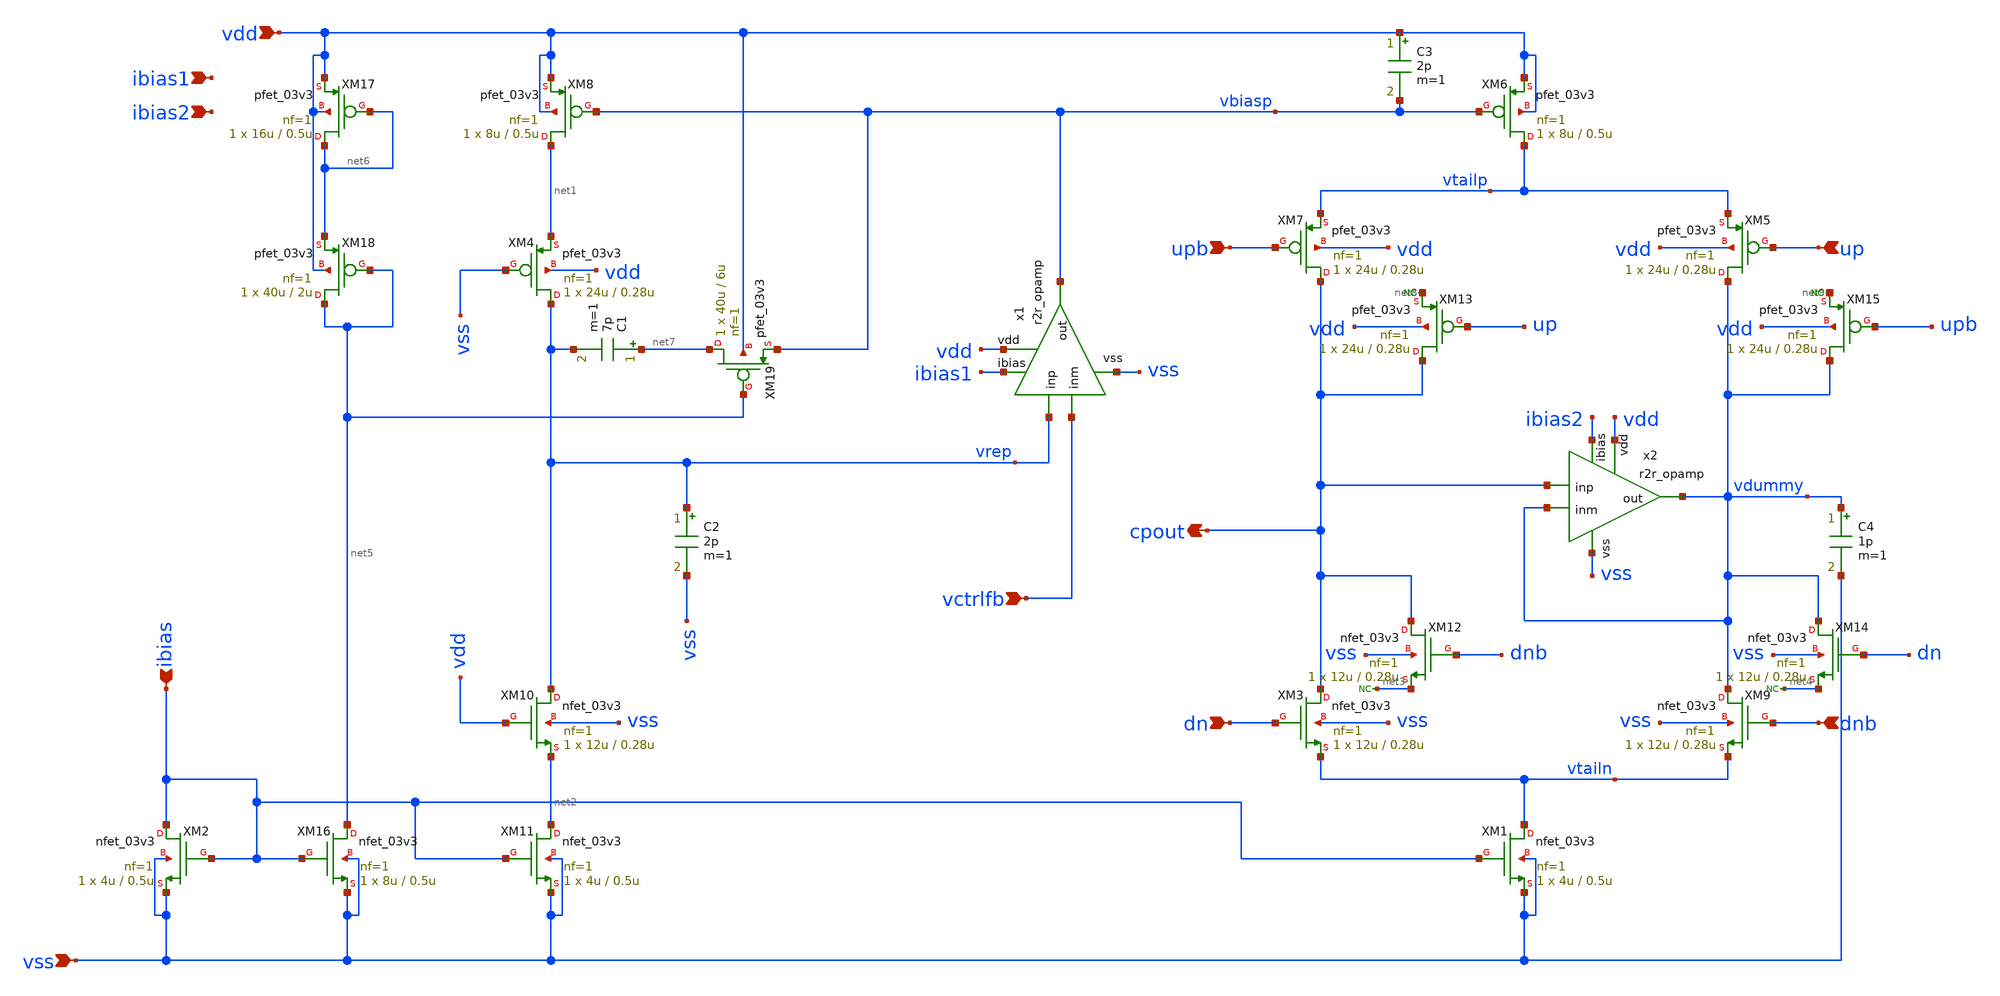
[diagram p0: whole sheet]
** sch_path: xschem/charge_pump_adv.sch
**.subckt charge_pump_adv vdd vss ibias dn upb up dnb cpout ibias1 ibias2 vctrlfb
*.ipin vdd
*.ipin vss
*.ipin ibias
*.ipin dn
*.ipin upb
*.ipin up
*.ipin dnb
*.opin cpout
*.ipin ibias1
*.ipin ibias2
*.ipin vctrlfb
XM1 vtailn ibias vss vss nfet_03v3 L=0.5u W=4u nf=1 ad='int((nf+1)/2) * W/nf * 0.18u' as='int((nf+2)/2) * W/nf * 0.18u'
+ pd='2*int((nf+1)/2) * (W/nf + 0.18u)' ps='2*int((nf+2)/2) * (W/nf + 0.18u)' nrd='0.18u / W' nrs='0.18u / W'
+ sa=0 sb=0 sd=0 m=1
XM2 ibias ibias vss vss nfet_03v3 L=0.5u W=4u nf=1 ad='int((nf+1)/2) * W/nf * 0.18u' as='int((nf+2)/2) * W/nf * 0.18u'
+ pd='2*int((nf+1)/2) * (W/nf + 0.18u)' ps='2*int((nf+2)/2) * (W/nf + 0.18u)' nrd='0.18u / W' nrs='0.18u / W'
+ sa=0 sb=0 sd=0 m=1
XM3 cpout dn vtailn vss nfet_03v3 L=0.28u W=12u nf=1 ad='int((nf+1)/2) * W/nf * 0.18u' as='int((nf+2)/2) * W/nf * 0.18u'
+ pd='2*int((nf+1)/2) * (W/nf + 0.18u)' ps='2*int((nf+2)/2) * (W/nf + 0.18u)' nrd='0.18u / W' nrs='0.18u / W'
+ sa=0 sb=0 sd=0 m=1
XM6 vtailp vbiasp vdd vdd pfet_03v3 L=0.5u W=8u nf=1 ad='int((nf+1)/2) * W/nf * 0.18u' as='int((nf+2)/2) * W/nf * 0.18u'
+ pd='2*int((nf+1)/2) * (W/nf + 0.18u)' ps='2*int((nf+2)/2) * (W/nf + 0.18u)' nrd='0.18u / W' nrs='0.18u / W'
+ sa=0 sb=0 sd=0 m=1
XM7 cpout upb vtailp vdd pfet_03v3 L=0.28u W=24u nf=1 ad='int((nf+1)/2) * W/nf * 0.18u' as='int((nf+2)/2) * W/nf * 0.18u'
+ pd='2*int((nf+1)/2) * (W/nf + 0.18u)' ps='2*int((nf+2)/2) * (W/nf + 0.18u)' nrd='0.18u / W' nrs='0.18u / W'
+ sa=0 sb=0 sd=0 m=1
XM8 net1 vbiasp vdd vdd pfet_03v3 L=0.5u W=8u nf=1 ad='int((nf+1)/2) * W/nf * 0.18u' as='int((nf+2)/2) * W/nf * 0.18u'
+ pd='2*int((nf+1)/2) * (W/nf + 0.18u)' ps='2*int((nf+2)/2) * (W/nf + 0.18u)' nrd='0.18u / W' nrs='0.18u / W'
+ sa=0 sb=0 sd=0 m=1
x1 vdd vbiasp ibias1 vrep vctrlfb vss r2r_opamp
XM5 vdummy up vtailp vdd pfet_03v3 L=0.28u W=24u nf=1 ad='int((nf+1)/2) * W/nf * 0.18u' as='int((nf+2)/2) * W/nf * 0.18u'
+ pd='2*int((nf+1)/2) * (W/nf + 0.18u)' ps='2*int((nf+2)/2) * (W/nf + 0.18u)' nrd='0.18u / W' nrs='0.18u / W'
+ sa=0 sb=0 sd=0 m=1
XM9 vdummy dnb vtailn vss nfet_03v3 L=0.28u W=12u nf=1 ad='int((nf+1)/2) * W/nf * 0.18u' as='int((nf+2)/2) * W/nf * 0.18u'
+ pd='2*int((nf+1)/2) * (W/nf + 0.18u)' ps='2*int((nf+2)/2) * (W/nf + 0.18u)' nrd='0.18u / W' nrs='0.18u / W'
+ sa=0 sb=0 sd=0 m=1
x2 vdd vdummy ibias2 cpout vdummy vss r2r_opamp
XM4 vrep vss net1 vdd pfet_03v3 L=0.28u W=24u nf=1 ad='int((nf+1)/2) * W/nf * 0.18u' as='int((nf+2)/2) * W/nf * 0.18u'
+ pd='2*int((nf+1)/2) * (W/nf + 0.18u)' ps='2*int((nf+2)/2) * (W/nf + 0.18u)' nrd='0.18u / W' nrs='0.18u / W'
+ sa=0 sb=0 sd=0 m=1
XM10 vrep vdd net2 vss nfet_03v3 L=0.28u W=12u nf=1 ad='int((nf+1)/2) * W/nf * 0.18u' as='int((nf+2)/2) * W/nf * 0.18u'
+ pd='2*int((nf+1)/2) * (W/nf + 0.18u)' ps='2*int((nf+2)/2) * (W/nf + 0.18u)' nrd='0.18u / W' nrs='0.18u / W'
+ sa=0 sb=0 sd=0 m=1
XM11 net2 ibias vss vss nfet_03v3 L=0.5u W=4u nf=1 ad='int((nf+1)/2) * W/nf * 0.18u' as='int((nf+2)/2) * W/nf * 0.18u'
+ pd='2*int((nf+1)/2) * (W/nf + 0.18u)' ps='2*int((nf+2)/2) * (W/nf + 0.18u)' nrd='0.18u / W' nrs='0.18u / W'
+ sa=0 sb=0 sd=0 m=1
XM12 cpout dnb net3 vss nfet_03v3 L=0.28u W=12u nf=1 ad='int((nf+1)/2) * W/nf * 0.18u' as='int((nf+2)/2) * W/nf * 0.18u'
+ pd='2*int((nf+1)/2) * (W/nf + 0.18u)' ps='2*int((nf+2)/2) * (W/nf + 0.18u)' nrd='0.18u / W' nrs='0.18u / W'
+ sa=0 sb=0 sd=0 m=1
XM13 cpout up net8 vdd pfet_03v3 L=0.28u W=24u nf=1 ad='int((nf+1)/2) * W/nf * 0.18u' as='int((nf+2)/2) * W/nf * 0.18u'
+ pd='2*int((nf+1)/2) * (W/nf + 0.18u)' ps='2*int((nf+2)/2) * (W/nf + 0.18u)' nrd='0.18u / W' nrs='0.18u / W'
+ sa=0 sb=0 sd=0 m=1
C1 net7 vrep 7p m=1
C4 vdummy vss 1p m=1
C3 vdd vbiasp 2p m=1
XM14 vdummy dn net4 vss nfet_03v3 L=0.28u W=12u nf=1 ad='int((nf+1)/2) * W/nf * 0.18u' as='int((nf+2)/2) * W/nf * 0.18u'
+ pd='2*int((nf+1)/2) * (W/nf + 0.18u)' ps='2*int((nf+2)/2) * (W/nf + 0.18u)' nrd='0.18u / W' nrs='0.18u / W'
+ sa=0 sb=0 sd=0 m=1
XM15 vdummy upb net9 vdd pfet_03v3 L=0.28u W=24u nf=1 ad='int((nf+1)/2) * W/nf * 0.18u' as='int((nf+2)/2) * W/nf * 0.18u'
+ pd='2*int((nf+1)/2) * (W/nf + 0.18u)' ps='2*int((nf+2)/2) * (W/nf + 0.18u)' nrd='0.18u / W' nrs='0.18u / W'
+ sa=0 sb=0 sd=0 m=1
* noconn #net3
* noconn #net4
* noconn #net9
* noconn #net8
XM16 net5 ibias vss vss nfet_03v3 L=0.5u W=8u nf=1 ad='int((nf+1)/2) * W/nf * 0.18u' as='int((nf+2)/2) * W/nf * 0.18u'
+ pd='2*int((nf+1)/2) * (W/nf + 0.18u)' ps='2*int((nf+2)/2) * (W/nf + 0.18u)' nrd='0.18u / W' nrs='0.18u / W'
+ sa=0 sb=0 sd=0 m=1
XM17 net6 net6 vdd vdd pfet_03v3 L=0.5u W=16u nf=1 ad='int((nf+1)/2) * W/nf * 0.18u' as='int((nf+2)/2) * W/nf * 0.18u'
+ pd='2*int((nf+1)/2) * (W/nf + 0.18u)' ps='2*int((nf+2)/2) * (W/nf + 0.18u)' nrd='0.18u / W' nrs='0.18u / W'
+ sa=0 sb=0 sd=0 m=1
XM18 net5 net5 net6 vdd pfet_03v3 L=2u W=40u nf=1 ad='int((nf+1)/2) * W/nf * 0.18u' as='int((nf+2)/2) * W/nf * 0.18u'
+ pd='2*int((nf+1)/2) * (W/nf + 0.18u)' ps='2*int((nf+2)/2) * (W/nf + 0.18u)' nrd='0.18u / W' nrs='0.18u / W'
+ sa=0 sb=0 sd=0 m=1
XM19 net7 net5 vbiasp vdd pfet_03v3 L=6u W=40u nf=1 ad='int((nf+1)/2) * W/nf * 0.18u' as='int((nf+2)/2) * W/nf * 0.18u'
+ pd='2*int((nf+1)/2) * (W/nf + 0.18u)' ps='2*int((nf+2)/2) * (W/nf + 0.18u)' nrd='0.18u / W' nrs='0.18u / W'
+ sa=0 sb=0 sd=0 m=1
C2 vrep vss 2p m=1
**.ends

* expanding   symbol:  r2r_opamp.sym # of pins=6
** sym_path: xschem/r2r_opamp.sym
** sch_path: xschem/r2r_opamp.sch
.subckt r2r_opamp vdd out ibias inp inm vss
*.ipin vss
*.ipin vdd
*.ipin ibias
*.ipin inp
*.ipin inm
*.opin out
XM1 net3 inp net8 vss nfet_03v3 L=0.28u W=16u nf=1 ad='int((nf+1)/2) * W/nf * 0.18u' as='int((nf+2)/2) * W/nf * 0.18u'
+ pd='2*int((nf+1)/2) * (W/nf + 0.18u)' ps='2*int((nf+2)/2) * (W/nf + 0.18u)' nrd='0.18u / W' nrs='0.18u / W'
+ sa=0 sb=0 sd=0 m=1
XM2 net4 inm net8 vss nfet_03v3 L=0.28u W=16u nf=1 ad='int((nf+1)/2) * W/nf * 0.18u' as='int((nf+2)/2) * W/nf * 0.18u'
+ pd='2*int((nf+1)/2) * (W/nf + 0.18u)' ps='2*int((nf+2)/2) * (W/nf + 0.18u)' nrd='0.18u / W' nrs='0.18u / W'
+ sa=0 sb=0 sd=0 m=1
XM3 net8 ibias vss vss nfet_03v3 L=0.5u W=16u nf=1 ad='int((nf+1)/2) * W/nf * 0.18u' as='int((nf+2)/2) * W/nf * 0.18u'
+ pd='2*int((nf+1)/2) * (W/nf + 0.18u)' ps='2*int((nf+2)/2) * (W/nf + 0.18u)' nrd='0.18u / W' nrs='0.18u / W'
+ sa=0 sb=0 sd=0 m=1
XM4 net6 inp net1 vdd pfet_03v3 L=0.28u W=32u nf=1 ad='int((nf+1)/2) * W/nf * 0.18u' as='int((nf+2)/2) * W/nf * 0.18u'
+ pd='2*int((nf+1)/2) * (W/nf + 0.18u)' ps='2*int((nf+2)/2) * (W/nf + 0.18u)' nrd='0.18u / W' nrs='0.18u / W'
+ sa=0 sb=0 sd=0 m=1
XM5 net7 inm net1 vdd pfet_03v3 L=0.28u W=32u nf=1 ad='int((nf+1)/2) * W/nf * 0.18u' as='int((nf+2)/2) * W/nf * 0.18u'
+ pd='2*int((nf+1)/2) * (W/nf + 0.18u)' ps='2*int((nf+2)/2) * (W/nf + 0.18u)' nrd='0.18u / W' nrs='0.18u / W'
+ sa=0 sb=0 sd=0 m=1
XM6 net1 net2 vdd vdd pfet_03v3 L=0.5u W=32u nf=1 ad='int((nf+1)/2) * W/nf * 0.18u' as='int((nf+2)/2) * W/nf * 0.18u'
+ pd='2*int((nf+1)/2) * (W/nf + 0.18u)' ps='2*int((nf+2)/2) * (W/nf + 0.18u)' nrd='0.18u / W' nrs='0.18u / W'
+ sa=0 sb=0 sd=0 m=1
XM7 net5 vbiasn net6 vss nfet_03v3 L=0.5u W=8u nf=1 ad='int((nf+1)/2) * W/nf * 0.18u' as='int((nf+2)/2) * W/nf * 0.18u'
+ pd='2*int((nf+1)/2) * (W/nf + 0.18u)' ps='2*int((nf+2)/2) * (W/nf + 0.18u)' nrd='0.18u / W' nrs='0.18u / W'
+ sa=0 sb=0 sd=0 m=1
XM8 out vbiasn net7 vss nfet_03v3 L=0.5u W=8u nf=1 ad='int((nf+1)/2) * W/nf * 0.18u' as='int((nf+2)/2) * W/nf * 0.18u'
+ pd='2*int((nf+1)/2) * (W/nf + 0.18u)' ps='2*int((nf+2)/2) * (W/nf + 0.18u)' nrd='0.18u / W' nrs='0.18u / W'
+ sa=0 sb=0 sd=0 m=1
XM9 net6 ibias vss vss nfet_03v3 L=0.5u W=16u nf=1 ad='int((nf+1)/2) * W/nf * 0.18u' as='int((nf+2)/2) * W/nf * 0.18u'
+ pd='2*int((nf+1)/2) * (W/nf + 0.18u)' ps='2*int((nf+2)/2) * (W/nf + 0.18u)' nrd='0.18u / W' nrs='0.18u / W'
+ sa=0 sb=0 sd=0 m=1
XM10 net7 ibias vss vss nfet_03v3 L=0.5u W=16u nf=1 ad='int((nf+1)/2) * W/nf * 0.18u' as='int((nf+2)/2) * W/nf * 0.18u'
+ pd='2*int((nf+1)/2) * (W/nf + 0.18u)' ps='2*int((nf+2)/2) * (W/nf + 0.18u)' nrd='0.18u / W' nrs='0.18u / W'
+ sa=0 sb=0 sd=0 m=1
XM11 net5 vbiasp net3 vdd pfet_03v3 L=0.5u W=16u nf=1 ad='int((nf+1)/2) * W/nf * 0.18u' as='int((nf+2)/2) * W/nf * 0.18u'
+ pd='2*int((nf+1)/2) * (W/nf + 0.18u)' ps='2*int((nf+2)/2) * (W/nf + 0.18u)' nrd='0.18u / W' nrs='0.18u / W'
+ sa=0 sb=0 sd=0 m=1
XM12 out vbiasp net4 vdd pfet_03v3 L=0.5u W=16u nf=1 ad='int((nf+1)/2) * W/nf * 0.18u' as='int((nf+2)/2) * W/nf * 0.18u'
+ pd='2*int((nf+1)/2) * (W/nf + 0.18u)' ps='2*int((nf+2)/2) * (W/nf + 0.18u)' nrd='0.18u / W' nrs='0.18u / W'
+ sa=0 sb=0 sd=0 m=1
XM13 net3 net5 vdd vdd pfet_03v3 L=0.5u W=32u nf=1 ad='int((nf+1)/2) * W/nf * 0.18u' as='int((nf+2)/2) * W/nf * 0.18u'
+ pd='2*int((nf+1)/2) * (W/nf + 0.18u)' ps='2*int((nf+2)/2) * (W/nf + 0.18u)' nrd='0.18u / W' nrs='0.18u / W'
+ sa=0 sb=0 sd=0 m=1
XM14 net4 net5 vdd vdd pfet_03v3 L=0.5u W=32u nf=1 ad='int((nf+1)/2) * W/nf * 0.18u' as='int((nf+2)/2) * W/nf * 0.18u'
+ pd='2*int((nf+1)/2) * (W/nf + 0.18u)' ps='2*int((nf+2)/2) * (W/nf + 0.18u)' nrd='0.18u / W' nrs='0.18u / W'
+ sa=0 sb=0 sd=0 m=1
XM15 ibias ibias vss vss nfet_03v3 L=0.5u W=2u nf=1 ad='int((nf+1)/2) * W/nf * 0.18u' as='int((nf+2)/2) * W/nf * 0.18u'
+ pd='2*int((nf+1)/2) * (W/nf + 0.18u)' ps='2*int((nf+2)/2) * (W/nf + 0.18u)' nrd='0.18u / W' nrs='0.18u / W'
+ sa=0 sb=0 sd=0 m=1
XM16 net2 ibias vss vss nfet_03v3 L=0.5u W=2u nf=1 ad='int((nf+1)/2) * W/nf * 0.18u' as='int((nf+2)/2) * W/nf * 0.18u'
+ pd='2*int((nf+1)/2) * (W/nf + 0.18u)' ps='2*int((nf+2)/2) * (W/nf + 0.18u)' nrd='0.18u / W' nrs='0.18u / W'
+ sa=0 sb=0 sd=0 m=1
XM17 net2 net2 vdd vdd pfet_03v3 L=0.5u W=4u nf=1 ad='int((nf+1)/2) * W/nf * 0.18u' as='int((nf+2)/2) * W/nf * 0.18u'
+ pd='2*int((nf+1)/2) * (W/nf + 0.18u)' ps='2*int((nf+2)/2) * (W/nf + 0.18u)' nrd='0.18u / W' nrs='0.18u / W'
+ sa=0 sb=0 sd=0 m=1
XM18 vbiasp ibias vss vss nfet_03v3 L=0.5u W=8u nf=1 ad='int((nf+1)/2) * W/nf * 0.18u' as='int((nf+2)/2) * W/nf * 0.18u'
+ pd='2*int((nf+1)/2) * (W/nf + 0.18u)' ps='2*int((nf+2)/2) * (W/nf + 0.18u)' nrd='0.18u / W' nrs='0.18u / W'
+ sa=0 sb=0 sd=0 m=1
XM19 vbiasp vbiasp vdd vdd pfet_03v3 L=0.5u W=4u nf=1 ad='int((nf+1)/2) * W/nf * 0.18u' as='int((nf+2)/2) * W/nf * 0.18u'
+ pd='2*int((nf+1)/2) * (W/nf + 0.18u)' ps='2*int((nf+2)/2) * (W/nf + 0.18u)' nrd='0.18u / W' nrs='0.18u / W'
+ sa=0 sb=0 sd=0 m=1
XM20 vbiasn net2 vdd vdd pfet_03v3 L=0.5u W=16u nf=1 ad='int((nf+1)/2) * W/nf * 0.18u' as='int((nf+2)/2) * W/nf * 0.18u'
+ pd='2*int((nf+1)/2) * (W/nf + 0.18u)' ps='2*int((nf+2)/2) * (W/nf + 0.18u)' nrd='0.18u / W' nrs='0.18u / W'
+ sa=0 sb=0 sd=0 m=1
XM21 vbiasn vbiasn vss vss nfet_03v3 L=0.5u W=2u nf=1 ad='int((nf+1)/2) * W/nf * 0.18u' as='int((nf+2)/2) * W/nf * 0.18u'
+ pd='2*int((nf+1)/2) * (W/nf + 0.18u)' ps='2*int((nf+2)/2) * (W/nf + 0.18u)' nrd='0.18u / W' nrs='0.18u / W'
+ sa=0 sb=0 sd=0 m=1
.ends

.end
